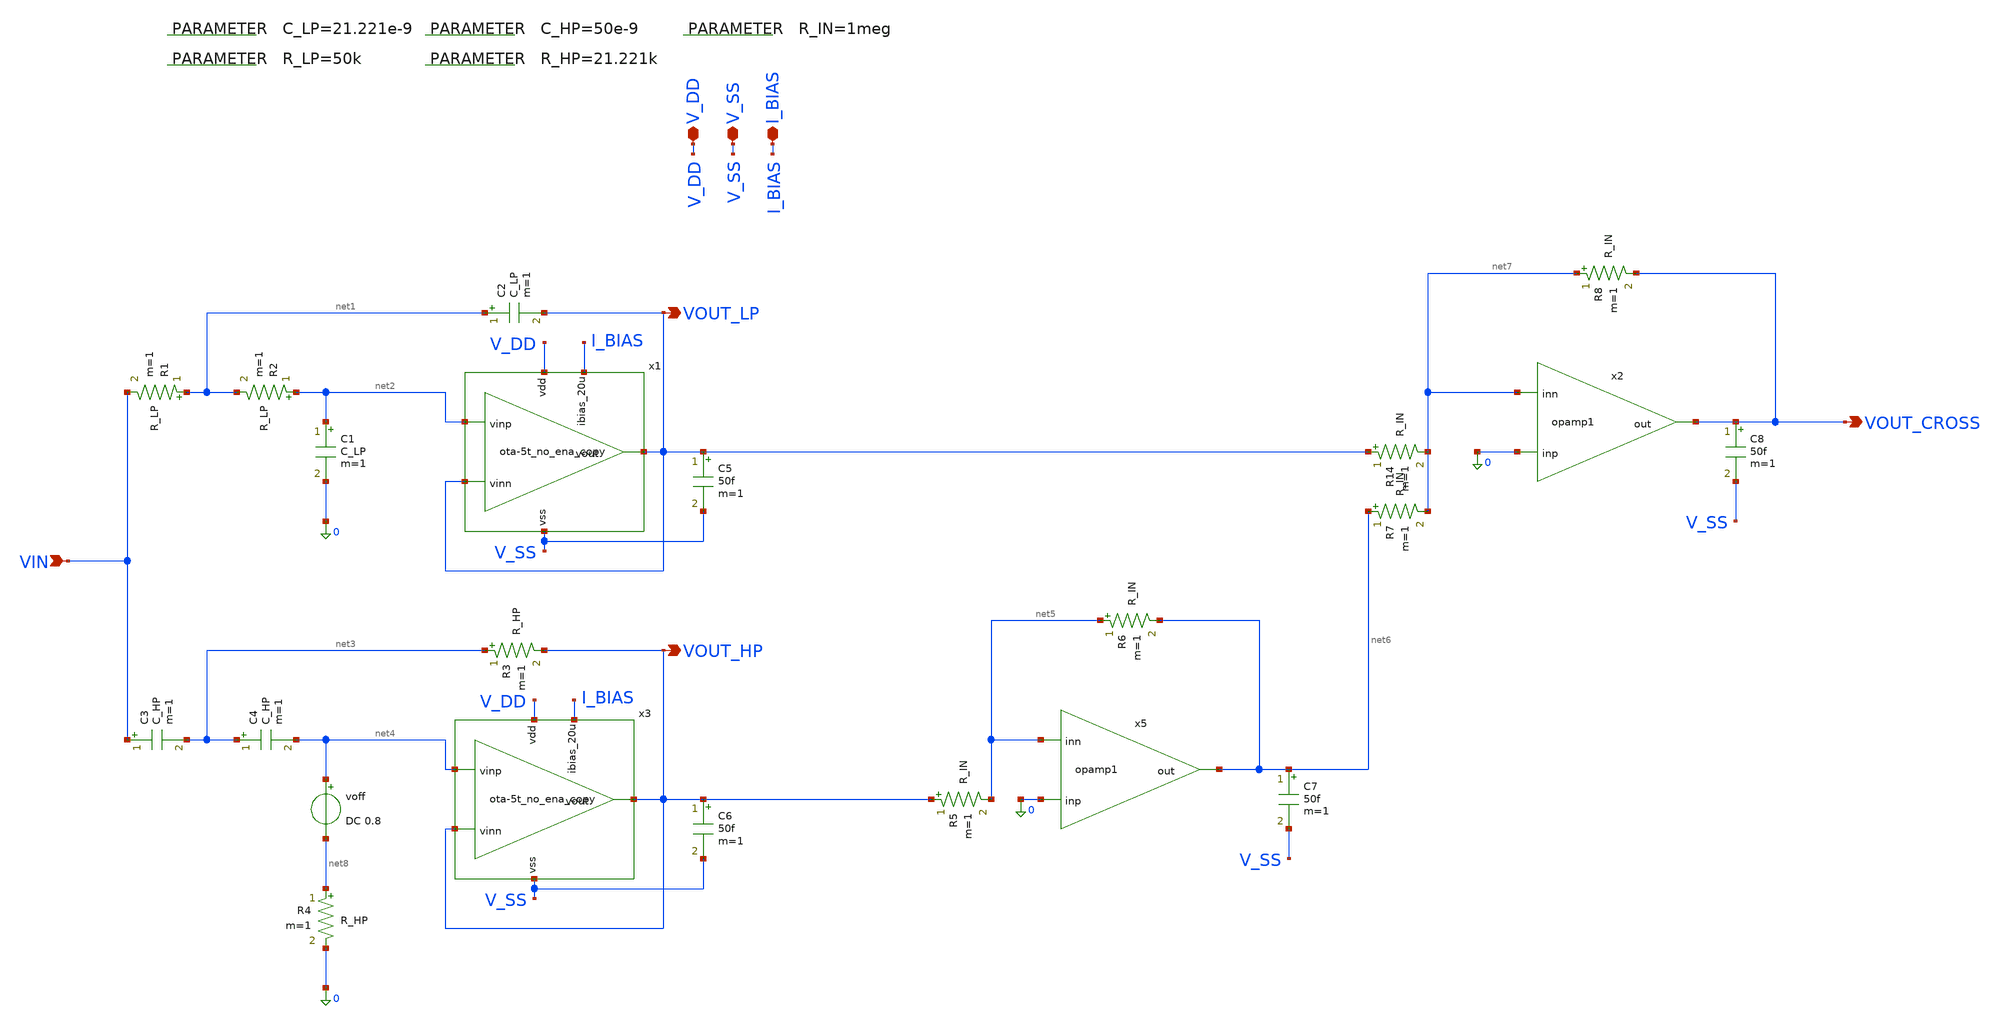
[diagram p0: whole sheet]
** sch_path: 004_Real_Circuits/002_version_no_enable/linkwtz_riley_crossover_pretl_OTA.sch
**.subckt linkwtz_riley_crossover_pretl_OTA VOUT_LP VIN V_DD VOUT_HP V_SS I_BIAS VOUT_CROSS
*.opin VOUT_LP
*.ipin VIN
*.iopin V_DD
*.opin VOUT_HP
*.iopin V_SS
*.iopin I_BIAS
*.opin VOUT_CROSS
R1 net1 VIN R_LP m=1
R2 net2 net1 R_LP m=1
C1 net2 0 C_LP m=1
C2 net1 VOUT_LP C_LP m=1
C3 VIN net3 C_HP m=1
C4 net3 net4 C_HP m=1
R3 net3 VOUT_HP R_HP m=1
R4 net8 0 R_HP m=1
R5 VOUT_HP net5 R_IN m=1
R6 net5 net6 R_IN m=1
R14 VOUT_LP net7 R_IN m=1
R7 net6 net7 R_IN m=1
R8 net7 VOUT_CROSS R_IN m=1
x1 V_DD VOUT_LP net2 VOUT_LP I_BIAS V_SS ota-5t_no_ena_copy
x3 V_DD VOUT_HP net4 VOUT_HP I_BIAS V_SS ota-5t_no_ena_copy
.param R_IN=1meg
.param C_LP=21.221e-9
.param R_LP=50k
.param C_HP=50e-9
.param R_HP=21.221k
C5 VOUT_LP V_SS 50f m=1
C6 VOUT_HP V_SS 50f m=1
C7 net6 V_SS 50f m=1
C8 VOUT_CROSS V_SS 50f m=1
voff net4 net8 DC 0.8
x5 0 net5 net6 opamp1
x2 0 net7 VOUT_CROSS opamp1
**.ends
.end
